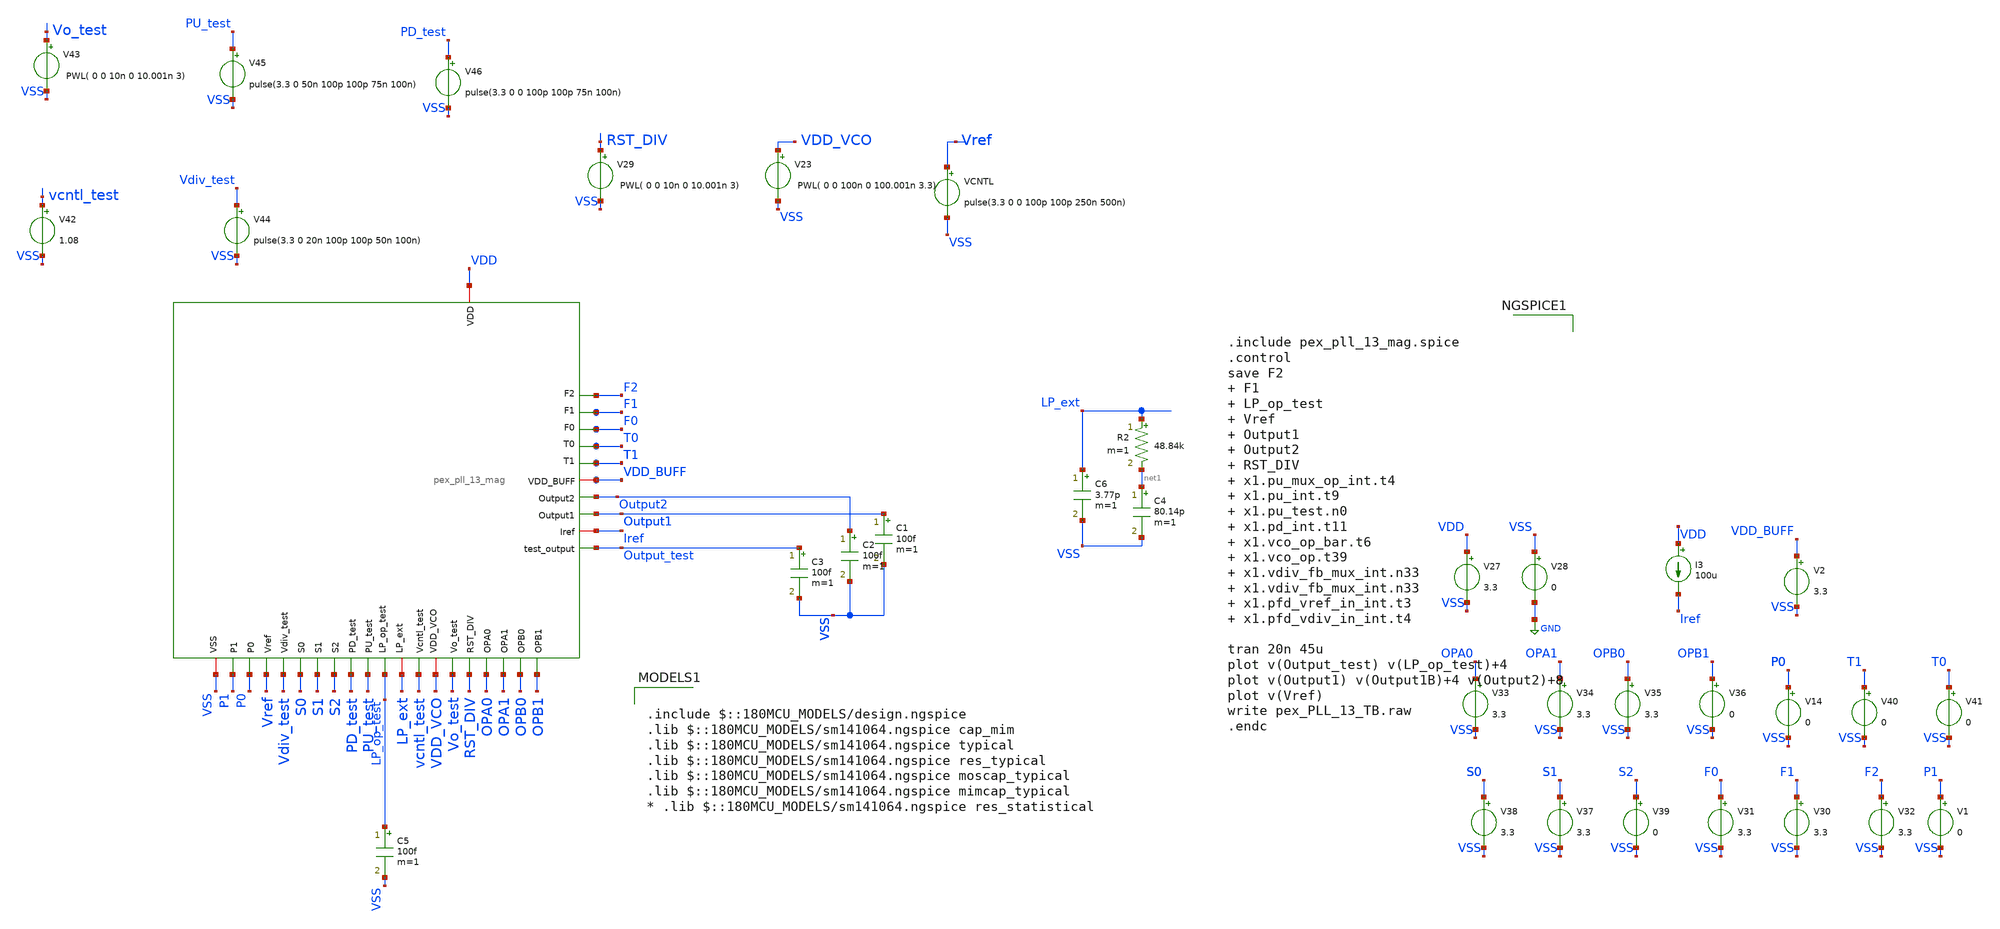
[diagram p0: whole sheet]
** sch_path: Clock_Generator_PAKISTAN_02/Schematics/pex_PLL_13_TB.sch
**.subckt pex_PLL_13_TB
C1 Output1 VSS 100f m=1
C2 Output2 VSS 100f m=1
C3 Output_test VSS 100f m=1
C5 LP_op_test VSS 100f m=1
C4 net1 VSS 80.14p m=1
C6 LP_ext VSS 3.77p m=1
R2 LP_ext net1 48.84k m=1
V1 P1 VSS 0
V14 P0 VSS 0
VCNTL Vref VSS pulse(3.3 0 0 100p 100p 250n 500n)
V23 VDD_VCO VSS PWL( 0 0 100n 0 100.001n 3.3)
V27 VDD VSS 3.3
V28 VSS GND 0
V29 RST_DIV VSS PWL( 0 0 10n 0 10.001n 3)
V30 F1 VSS 3.3
V31 F0 VSS 3.3
V32 F2 VSS 3.3
V33 OPA0 VSS 3.3
V34 OPA1 VSS 3.3
V35 OPB0 VSS 3.3
V36 OPB1 VSS 0
I3 VDD Iref 100u
V37 S1 VSS 3.3
V38 S0 VSS 3.3
V39 S2 VSS 0
V40 T1 VSS 0
V41 T0 VSS 0
V42 vcntl_test VSS 1.08
V43 Vo_test VSS PWL( 0 0 10n 0 10.001n 3)
V44 Vdiv_test VSS pulse(3.3 0 20n 100p 100p 50n 100n)
V45 PU_test VSS pulse(3.3 0 50n 100p 100p 75n 100n)
V46 PD_test VSS pulse(3.3 0 0 100p 100p 75n 100n)
V2 VDD_BUFF VSS 3.3
x1 Iref LP_ext VDD_BUFF VDD VDD_VCO VSS RST_DIV Vref S2 T0 S0 S1 F2 F0 T1 F1 OPA1 OPA0 OPB1 P1 OPB0
+ P0 Vo_test PD_test vcntl_test PU_test Vdiv_test Output1 Output2 Output_test LP_op_test pex_pll_13_mag
**** begin user architecture code


.include pex_pll_13_mag.spice
.control
save F2  F1  LP_op_test  Vref  Output1  Output2  RST_DIV  x1.pu_mux_op_int.t4  x1.pu_int.t9
+  x1.pu_test.n0  x1.pd_int.t11  x1.vco_op_bar.t6  x1.vco_op.t39  x1.vdiv_fb_mux_int.n33  x1.vdiv_fb_mux_int.n33
+  x1.pfd_vref_in_int.t3  x1.pfd_vdiv_in_int.t4

tran 20n 45u
plot v(Output_test) v(LP_op_test)+4
plot v(Output1) v(Output1B)+4 v(Output2)+8
plot v(Vref)
write pex_PLL_13_TB.raw
.endc




.include $::180MCU_MODELS/design.ngspice
.lib $::180MCU_MODELS/sm141064.ngspice cap_mim
.lib $::180MCU_MODELS/sm141064.ngspice typical
.lib $::180MCU_MODELS/sm141064.ngspice res_typical
.lib $::180MCU_MODELS/sm141064.ngspice moscap_typical
.lib $::180MCU_MODELS/sm141064.ngspice mimcap_typical
* .lib $::180MCU_MODELS/sm141064.ngspice res_statistical

**** end user architecture code
**.ends
.GLOBAL GND
.end
